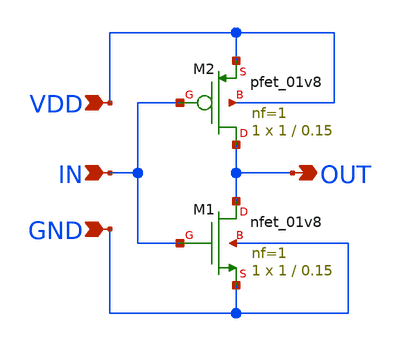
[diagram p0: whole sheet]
** sch_path: Inverter_RingOsc/inverter.sch
**.subckt inverter GND IN VDD OUT
*.ipin GND
*.ipin IN
*.ipin VDD
*.opin OUT
XM1 OUT IN GND GND sky130_fd_pr__nfet_01v8 L=0.15 W=1 nf=1 ad='int((nf+1)/2) * W/nf * 0.29' as='int((nf+2)/2) * W/nf * 0.29'
+ pd='2*int((nf+1)/2) * (W/nf + 0.29)' ps='2*int((nf+2)/2) * (W/nf + 0.29)' nrd='0.29 / W' nrs='0.29 / W'
+ sa=0 sb=0 sd=0 mult=1 m=1
XM2 OUT IN VDD VDD sky130_fd_pr__pfet_01v8 L=0.15 W=1 nf=1 ad='int((nf+1)/2) * W/nf * 0.29' as='int((nf+2)/2) * W/nf * 0.29'
+ pd='2*int((nf+1)/2) * (W/nf + 0.29)' ps='2*int((nf+2)/2) * (W/nf + 0.29)' nrd='0.29 / W' nrs='0.29 / W'
+ sa=0 sb=0 sd=0 mult=1 m=1
**.ends
.end
